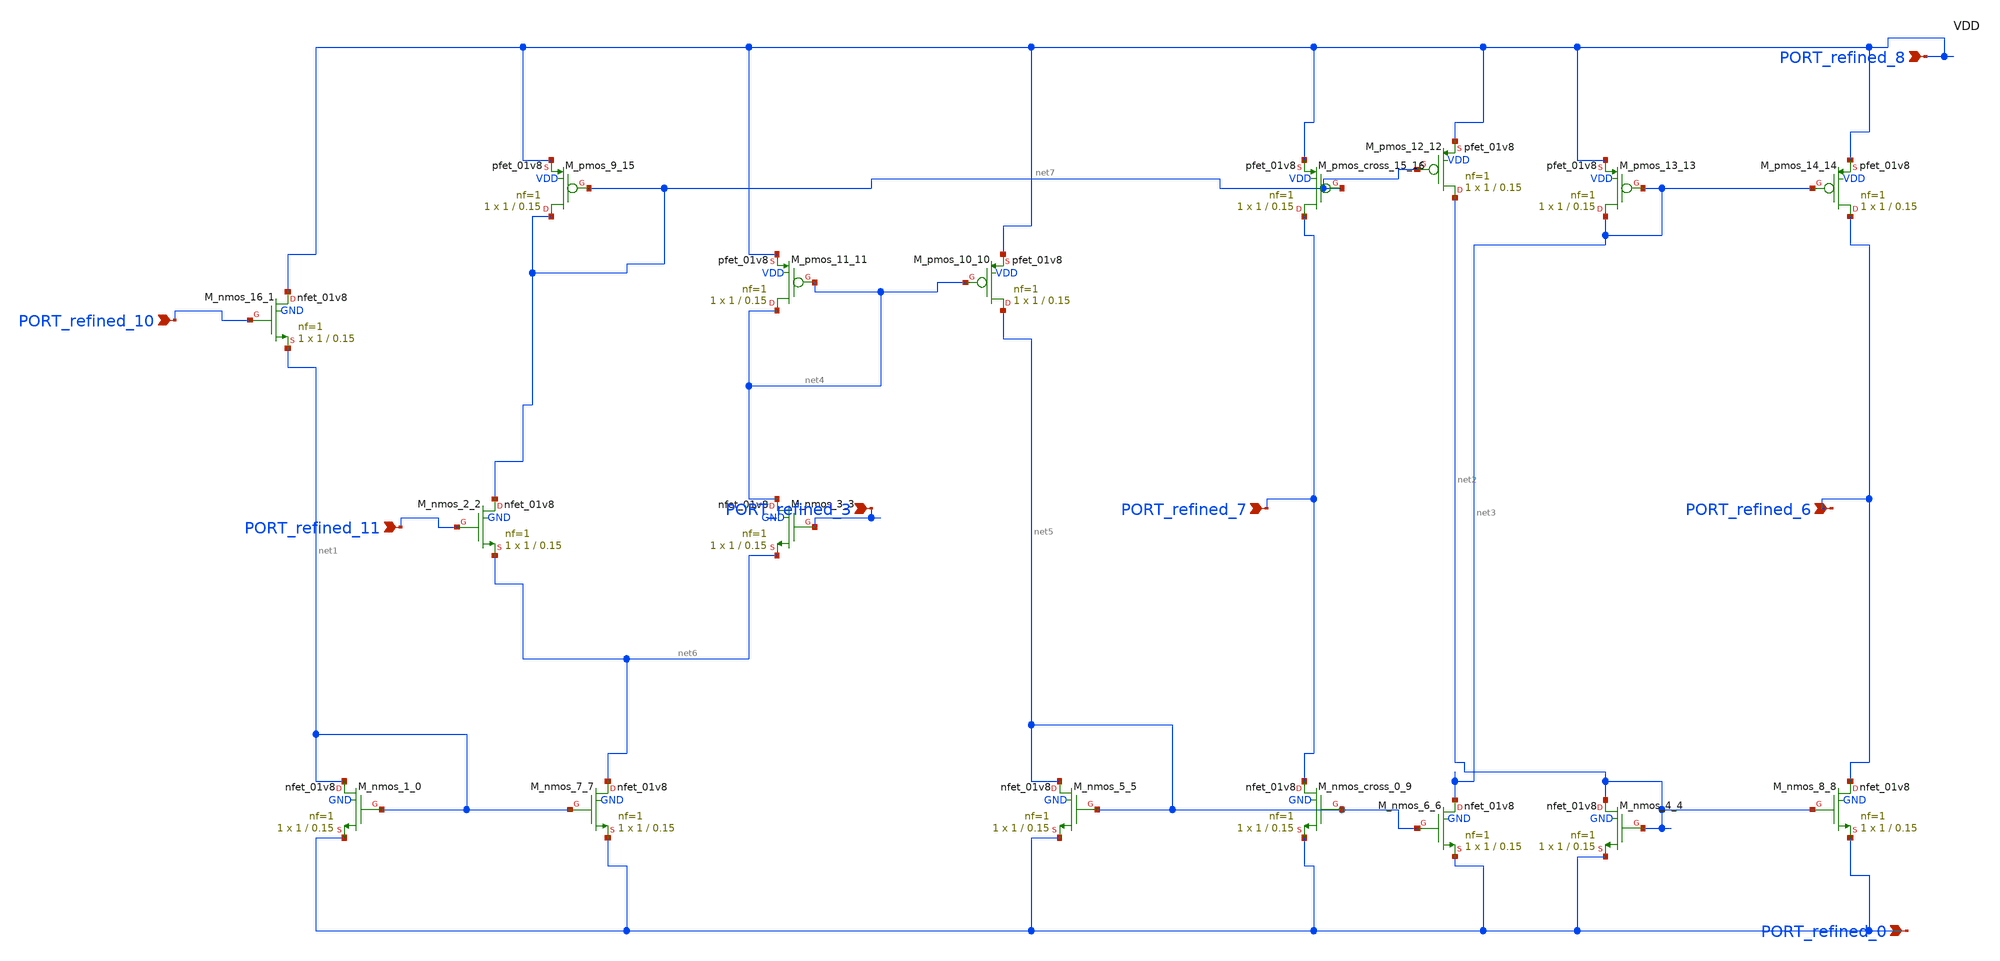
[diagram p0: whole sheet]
** sch_path: schematics/p05_fig1d_ota.sch
**.subckt p05_fig1d_ota PORT_refined_3 PORT_refined_10 PORT_refined_11 PORT_refined_0 PORT_refined_7
*+ PORT_refined_8 PORT_refined_6
*.ipin PORT_refined_3
*.ipin PORT_refined_10
*.ipin PORT_refined_11
*.ipin PORT_refined_0
*.ipin PORT_refined_7
*.ipin PORT_refined_8
*.ipin PORT_refined_6
XM_nmos_1_0 net1 net1 PORT_refined_0 GND sky130_fd_pr__nfet_01v8 L=0.15 W=1 nf=1 ad='int((1 + 1)/2) * 1 / 1 * 0.29'
+ as='int((1 + 2)/2) * 1 / 1 * 0.29' pd='2*int((1 + 1)/2) * (1 / 1 + 0.29)' ps='2*int((1 + 2)/2) * (1 / 1 + 0.29)'
+ nrd='0.29 / 1 ' nrs='0.29 / 1 ' sa=0 sb=0 sd=0 mult=1 m=1
XM_nmos_16_1 PORT_refined_8 PORT_refined_10 net1 GND sky130_fd_pr__nfet_01v8 L=0.15 W=1 nf=1 ad='int((1 + 1)/2) * 1 / 1 * 0.29'
+ as='int((1 + 2)/2) * 1 / 1 * 0.29' pd='2*int((1 + 1)/2) * (1 / 1 + 0.29)' ps='2*int((1 + 2)/2) * (1 / 1 + 0.29)'
+ nrd='0.29 / 1 ' nrs='0.29 / 1 ' sa=0 sb=0 sd=0 mult=1 m=1
XM_nmos_2_2 net7 PORT_refined_11 net6 GND sky130_fd_pr__nfet_01v8 L=0.15 W=1 nf=1 ad='int((1 + 1)/2) * 1 / 1 * 0.29'
+ as='int((1 + 2)/2) * 1 / 1 * 0.29' pd='2*int((1 + 1)/2) * (1 / 1 + 0.29)' ps='2*int((1 + 2)/2) * (1 / 1 + 0.29)'
+ nrd='0.29 / 1 ' nrs='0.29 / 1 ' sa=0 sb=0 sd=0 mult=1 m=1
XM_nmos_3_3 net4 PORT_refined_3 net6 GND sky130_fd_pr__nfet_01v8 L=0.15 W=1 nf=1 ad='int((1 + 1)/2) * 1 / 1 * 0.29'
+ as='int((1 + 2)/2) * 1 / 1 * 0.29' pd='2*int((1 + 1)/2) * (1 / 1 + 0.29)' ps='2*int((1 + 2)/2) * (1 / 1 + 0.29)'
+ nrd='0.29 / 1 ' nrs='0.29 / 1 ' sa=0 sb=0 sd=0 mult=1 m=1
XM_nmos_4_4 net2 net2 PORT_refined_0 GND sky130_fd_pr__nfet_01v8 L=0.15 W=1 nf=1 ad='int((1 + 1)/2) * 1 / 1 * 0.29'
+ as='int((1 + 2)/2) * 1 / 1 * 0.29' pd='2*int((1 + 1)/2) * (1 / 1 + 0.29)' ps='2*int((1 + 2)/2) * (1 / 1 + 0.29)'
+ nrd='0.29 / 1 ' nrs='0.29 / 1 ' sa=0 sb=0 sd=0 mult=1 m=1
XM_nmos_5_5 net5 net5 PORT_refined_0 GND sky130_fd_pr__nfet_01v8 L=0.15 W=1 nf=1 ad='int((1 + 1)/2) * 1 / 1 * 0.29'
+ as='int((1 + 2)/2) * 1 / 1 * 0.29' pd='2*int((1 + 1)/2) * (1 / 1 + 0.29)' ps='2*int((1 + 2)/2) * (1 / 1 + 0.29)'
+ nrd='0.29 / 1 ' nrs='0.29 / 1 ' sa=0 sb=0 sd=0 mult=1 m=1
XM_nmos_6_6 net3 net5 PORT_refined_0 GND sky130_fd_pr__nfet_01v8 L=0.15 W=1 nf=1 ad='int((1 + 1)/2) * 1 / 1 * 0.29'
+ as='int((1 + 2)/2) * 1 / 1 * 0.29' pd='2*int((1 + 1)/2) * (1 / 1 + 0.29)' ps='2*int((1 + 2)/2) * (1 / 1 + 0.29)'
+ nrd='0.29 / 1 ' nrs='0.29 / 1 ' sa=0 sb=0 sd=0 mult=1 m=1
XM_nmos_7_7 net6 net1 PORT_refined_0 GND sky130_fd_pr__nfet_01v8 L=0.15 W=1 nf=1 ad='int((1 + 1)/2) * 1 / 1 * 0.29'
+ as='int((1 + 2)/2) * 1 / 1 * 0.29' pd='2*int((1 + 1)/2) * (1 / 1 + 0.29)' ps='2*int((1 + 2)/2) * (1 / 1 + 0.29)'
+ nrd='0.29 / 1 ' nrs='0.29 / 1 ' sa=0 sb=0 sd=0 mult=1 m=1
XM_nmos_8_8 PORT_refined_6 net2 PORT_refined_0 GND sky130_fd_pr__nfet_01v8 L=0.15 W=1 nf=1 ad='int((1 + 1)/2) * 1 / 1 * 0.29'
+ as='int((1 + 2)/2) * 1 / 1 * 0.29' pd='2*int((1 + 1)/2) * (1 / 1 + 0.29)' ps='2*int((1 + 2)/2) * (1 / 1 + 0.29)'
+ nrd='0.29 / 1 ' nrs='0.29 / 1 ' sa=0 sb=0 sd=0 mult=1 m=1
XM_nmos_cross_0_9 PORT_refined_7 net5 PORT_refined_0 GND sky130_fd_pr__nfet_01v8 L=0.15 W=1 nf=1 ad='int((1 + 1)/2) * 1 / 1 * 0.29'
+ as='int((1 + 2)/2) * 1 / 1 * 0.29' pd='2*int((1 + 1)/2) * (1 / 1 + 0.29)' ps='2*int((1 + 2)/2) * (1 / 1 + 0.29)'
+ nrd='0.29 / 1 ' nrs='0.29 / 1 ' sa=0 sb=0 sd=0 mult=1 m=1
XM_pmos_10_10 net5 net4 PORT_refined_8 VDD sky130_fd_pr__pfet_01v8 L=0.15 W=1 nf=1 ad='int((1 + 1)/2) * 1 / 1 * 0.29'
+ as='int((1 + 2)/2) * 1 / 1 * 0.29' pd='2*int((1 + 1)/2) * (1 / 1 + 0.29)' ps='2*int((1 + 2)/2) * (1 / 1 + 0.29)'
+ nrd='0.29 / 1 ' nrs='0.29 / 1 ' sa=0 sb=0 sd=0 mult=1 m=1
XM_pmos_11_11 net4 net4 PORT_refined_8 VDD sky130_fd_pr__pfet_01v8 L=0.15 W=1 nf=1 ad='int((1 + 1)/2) * 1 / 1 * 0.29'
+ as='int((1 + 2)/2) * 1 / 1 * 0.29' pd='2*int((1 + 1)/2) * (1 / 1 + 0.29)' ps='2*int((1 + 2)/2) * (1 / 1 + 0.29)'
+ nrd='0.29 / 1 ' nrs='0.29 / 1 ' sa=0 sb=0 sd=0 mult=1 m=1
XM_pmos_12_12 net2 net7 PORT_refined_8 VDD sky130_fd_pr__pfet_01v8 L=0.15 W=1 nf=1 ad='int((1 + 1)/2) * 1 / 1 * 0.29'
+ as='int((1 + 2)/2) * 1 / 1 * 0.29' pd='2*int((1 + 1)/2) * (1 / 1 + 0.29)' ps='2*int((1 + 2)/2) * (1 / 1 + 0.29)'
+ nrd='0.29 / 1 ' nrs='0.29 / 1 ' sa=0 sb=0 sd=0 mult=1 m=1
XM_pmos_13_13 net3 net3 PORT_refined_8 VDD sky130_fd_pr__pfet_01v8 L=0.15 W=1 nf=1 ad='int((1 + 1)/2) * 1 / 1 * 0.29'
+ as='int((1 + 2)/2) * 1 / 1 * 0.29' pd='2*int((1 + 1)/2) * (1 / 1 + 0.29)' ps='2*int((1 + 2)/2) * (1 / 1 + 0.29)'
+ nrd='0.29 / 1 ' nrs='0.29 / 1 ' sa=0 sb=0 sd=0 mult=1 m=1
XM_pmos_14_14 PORT_refined_6 net3 PORT_refined_8 VDD sky130_fd_pr__pfet_01v8 L=0.15 W=1 nf=1 ad='int((1 + 1)/2) * 1 / 1 * 0.29'
+ as='int((1 + 2)/2) * 1 / 1 * 0.29' pd='2*int((1 + 1)/2) * (1 / 1 + 0.29)' ps='2*int((1 + 2)/2) * (1 / 1 + 0.29)'
+ nrd='0.29 / 1 ' nrs='0.29 / 1 ' sa=0 sb=0 sd=0 mult=1 m=1
XM_pmos_9_15 net7 net7 PORT_refined_8 VDD sky130_fd_pr__pfet_01v8 L=0.15 W=1 nf=1 ad='int((1 + 1)/2) * 1 / 1 * 0.29'
+ as='int((1 + 2)/2) * 1 / 1 * 0.29' pd='2*int((1 + 1)/2) * (1 / 1 + 0.29)' ps='2*int((1 + 2)/2) * (1 / 1 + 0.29)'
+ nrd='0.29 / 1 ' nrs='0.29 / 1 ' sa=0 sb=0 sd=0 mult=1 m=1
XM_pmos_cross_15_16 PORT_refined_7 net7 PORT_refined_8 VDD sky130_fd_pr__pfet_01v8 L=0.15 W=1 nf=1 ad='int((1 + 1)/2) * 1 / 1 * 0.29'
+ as='int((1 + 2)/2) * 1 / 1 * 0.29' pd='2*int((1 + 1)/2) * (1 / 1 + 0.29)' ps='2*int((1 + 2)/2) * (1 / 1 + 0.29)'
+ nrd='0.29 / 1 ' nrs='0.29 / 1 ' sa=0 sb=0 sd=0 mult=1 m=1
**.ends
.end
